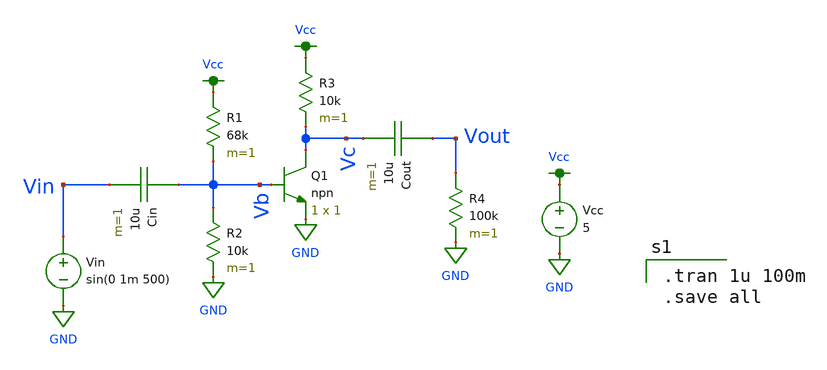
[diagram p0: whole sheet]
** sch_path: mp1/test2/bipolar_amplifier_backup.sch
**.subckt bipolar_amplifier_backup
Q1 Vc Vb GND npn area=1 m=1
R2 Vb GND 10k m=1
Cin Vb Vin 10u m=1
R1 Vcc Vb 68k m=1
R3 Vcc Vc 10k m=1
Cout Vout Vc 10u m=1
R4 Vout GND 100k m=1
Vcc Vcc GND 5
Vin Vin GND sin(0 1m 500)
**** begin user architecture code

.option wnflag=1
.lib ~/skywater/skywater-pdk/libraries/sky130_fd_pr_ngspice/latest/models/sky130.lib.spice tt


.tran 1u 100m
.save all

**** end user architecture code
**.ends
.GLOBAL GND
.GLOBAL Vcc
.end
